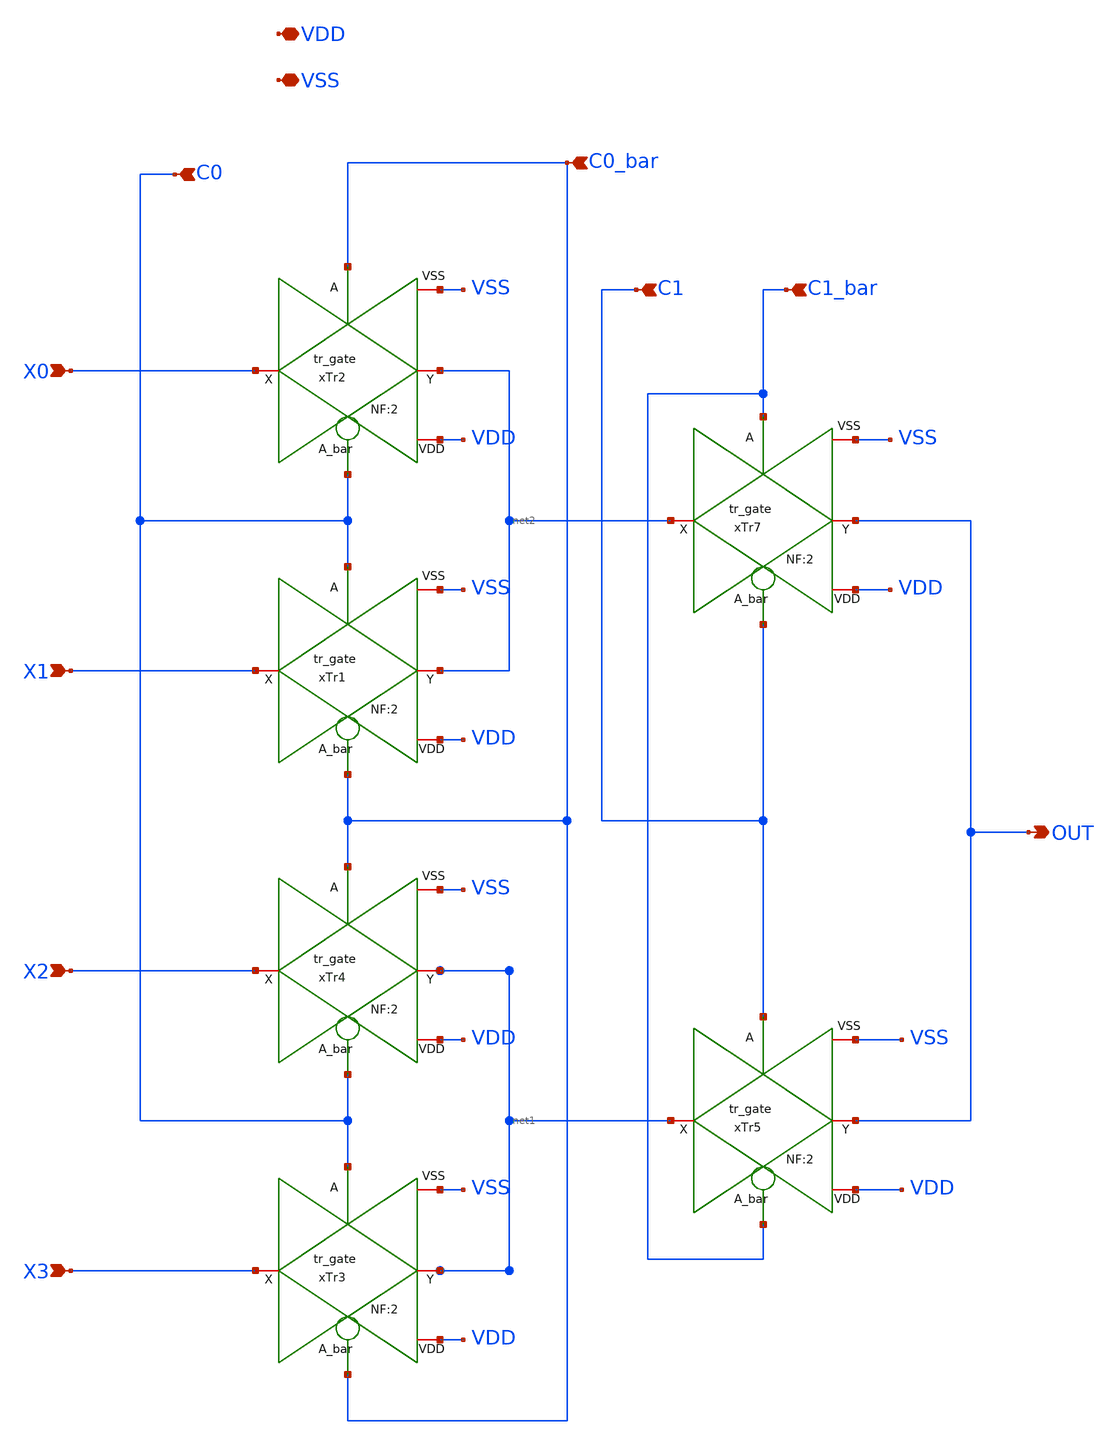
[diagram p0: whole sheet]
** sch_path: xschem_lib/DFFRAM_full_custom/mux4to1.sch
**.subckt mux4to1 C0 C0_bar C1_bar C1 X0 X1 X2 X3 OUT VDD VSS
*.ipin C0
*.ipin C0_bar
*.ipin C1_bar
*.ipin C1
*.ipin X0
*.ipin X1
*.ipin X2
*.ipin X3
*.opin OUT
*.iopin VDD
*.iopin VSS
xTr1 X1 VDD C0_bar VSS C0 net2 tr_gate NF=2
xTr2 X0 VDD C0 VSS C0_bar net2 tr_gate NF=2
xTr3 X3 VDD C0_bar VSS C0 net1 tr_gate NF=2
xTr4 X2 VDD C0 VSS C0_bar net1 tr_gate NF=2
xTr5 net1 VDD C1_bar VSS C1 OUT tr_gate NF=2
xTr7 net2 VDD C1 VSS C1_bar OUT tr_gate NF=2
**.ends

* expanding   symbol:  xschem_lib/DFFRAM_full_custom/tr_gate.sym # of pins=6
** sym_path: xschem_lib/DFFRAM_full_custom/tr_gate.sym
** sch_path: xschem_lib/DFFRAM_full_custom/tr_gate.sch
.subckt tr_gate X VDD A_bar VSS A Y  NF=2
*.iopin VSS
*.ipin A_bar
*.iopin VDD
*.ipin A
*.iopin X
*.iopin Y
XM1 X A Y VSS nfet_03v3 L=0.28u W=NF*0.85u nf=NF ad='int((nf+1)/2) * W/nf * 0.18u' as='int((nf+2)/2) * W/nf * 0.18u'
+ pd='2*int((nf+1)/2) * (W/nf + 0.18u)' ps='2*int((nf+2)/2) * (W/nf + 0.18u)' nrd='0.18u / W' nrs='0.18u / W'
+ sa=0 sb=0 sd=0 m=1
XM2 Y A_bar X VDD pfet_03v3 L=0.28u W=NF*1.7u nf=NF ad='int((nf+1)/2) * W/nf * 0.18u' as='int((nf+2)/2) * W/nf * 0.18u'
+ pd='2*int((nf+1)/2) * (W/nf + 0.18u)' ps='2*int((nf+2)/2) * (W/nf + 0.18u)' nrd='0.18u / W' nrs='0.18u / W'
+ sa=0 sb=0 sd=0 m=1
.ends

.end
